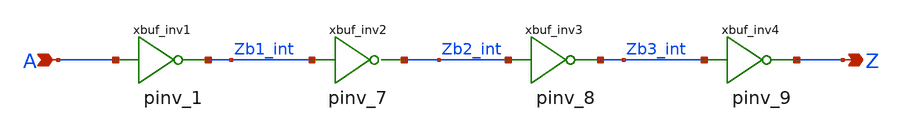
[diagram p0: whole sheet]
** sch_path: sram_2_64_scn4m_lcc/pdriver_1.sch
**.subckt pdriver_1 A Z
*.ipin A
*.opin Z
xbuf_inv1 A Zb1_int vdd gnd pinv_1
xbuf_inv2 Zb1_int Zb2_int vdd gnd pinv_7
xbuf_inv3 Zb2_int Zb3_int vdd gnd pinv_8
xbuf_inv4 Zb3_int Z vdd gnd pinv_9
**.ends

* expanding   symbol:  pinv_1.sym # of pins=2
** sym_path: sram_2_64_scn4m_lcc/pinv_1.sym
** sch_path: sram_2_64_scn4m_lcc/pinv_1.sch
.subckt pinv_1 A Z vdd gnd
*.ipin A
*.opin Z
Mpinv_nmos Z A gnd gnd n w=0.8u l=0.4u m=1
Mp_inv_pmos Z A vdd vdd p w=6.4u l=0.4u m=1
.ends


* expanding   symbol:  pinv_7.sym # of pins=2
** sym_path: sram_2_16_scn4m/pinv_7.sym
** sch_path: sram_2_16_scn4m/pinv_7.sch
.subckt pinv_7 A Z vdd gnd
*.ipin A
*.opin Z
Mpinv_nmos Z A gnd gnd n w=4.0u l=0.4u m=3
Mp_inv_pmos Z A vdd vdd p w=8.0u l=0.4u m=3
.ends


* expanding   symbol:  pinv_8.sym # of pins=2
** sym_path: sram_2_64_scn4m/pinv_8.sym
** sch_path: sram_2_64_scn4m/pinv_8.sch
.subckt pinv_8 A Z vdd gnd
*.ipin A
*.opin Z
XMpinv_nmos Z A gnd gnd sky130_fd_pr__nfet_01v8 L=0.4 W=2.8 nf=1 ad='int((nf+1)/2) * W/nf * 0.29' as='int((nf+2)/2) * W/nf * 0.29'
+ pd='2*int((nf+1)/2) * (W/nf + 0.29)' ps='2*int((nf+2)/2) * (W/nf + 0.29)' nrd='0.29 / W' nrs='0.29 / W'
+ sa=0 sb=0 sd=0 mult=1 m=1
XMp_inv_pmos Z A vdd vdd sky130_fd_pr__pfet_01v8 L=0.4 W=5.6 nf=1 ad='int((nf+1)/2) * W/nf * 0.29' as='int((nf+2)/2) * W/nf * 0.29'
+ pd='2*int((nf+1)/2) * (W/nf + 0.29)' ps='2*int((nf+2)/2) * (W/nf + 0.29)' nrd='0.29 / W' nrs='0.29 / W'
+ sa=0 sb=0 sd=0 mult=1 m=1
.ends


* expanding   symbol:  pinv_9.sym # of pins=2
** sym_path: sram_2_16_scn4m/pinv_9.sym
** sch_path: sram_2_16_scn4m/pinv_9.sch
.subckt pinv_9 A Z vdd gnd
*.ipin A
*.opin Z
Mpinv_nmos Z A gnd gnd n w=4.0u l=0.4u m=2
Mp_inv_pmos Z A vdd vdd p w=8.0u l=0.4u m=2
.ends

.end
